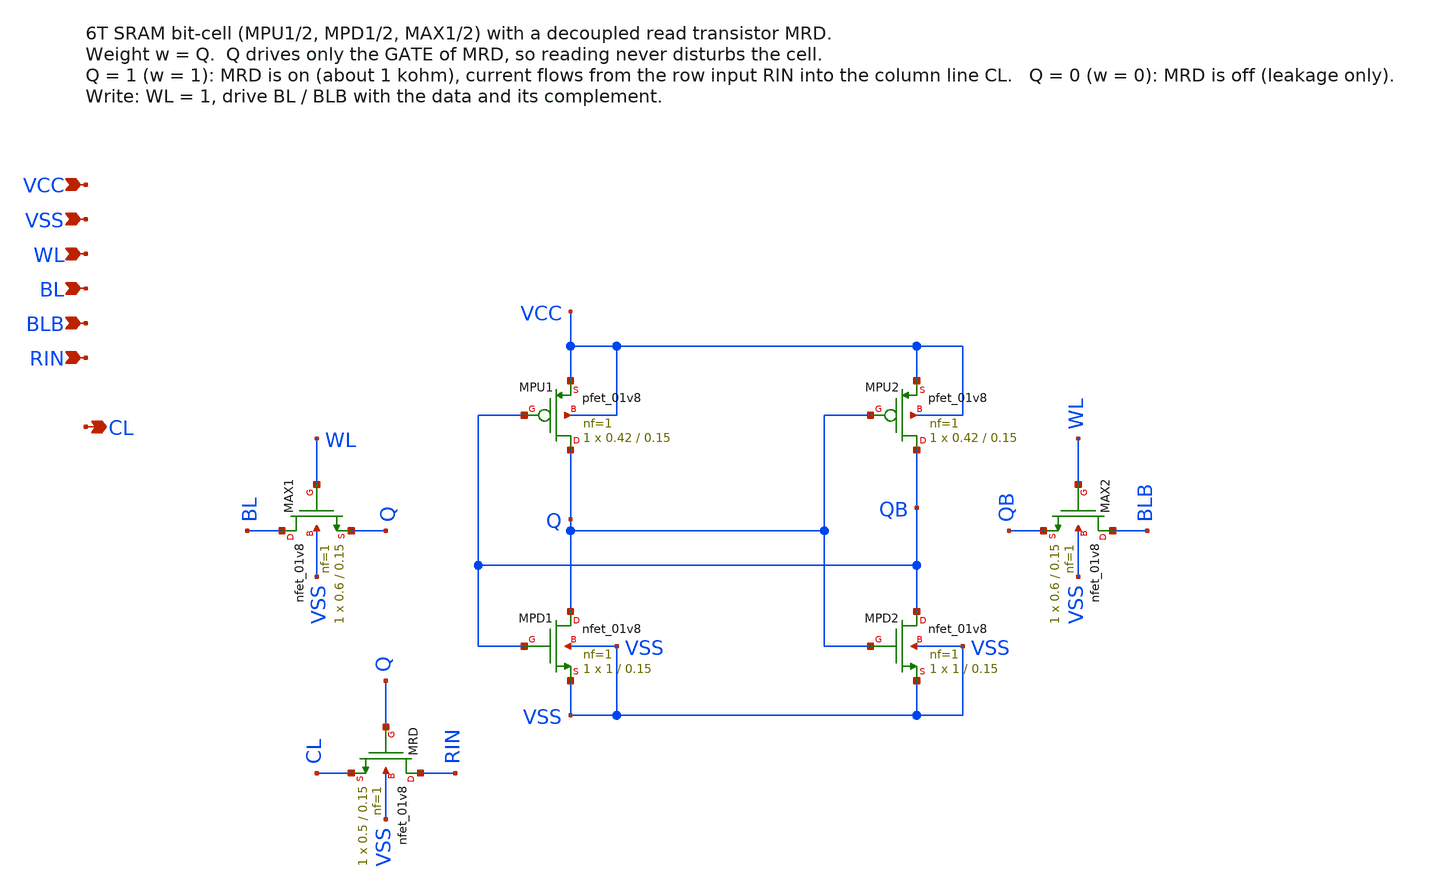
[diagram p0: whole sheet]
** sch_path: CiM components/sram_cell6t.sch
**.subckt sram_cell6t VCC VSS WL BL BLB RIN CL
*.ipin VCC
*.ipin VSS
*.ipin WL
*.ipin BL
*.ipin BLB
*.ipin RIN
*.opin CL
XMPU1 Q QB VCC VCC sky130_fd_pr__pfet_01v8 L=0.15 W=0.42 nf=1 ad='int((nf+1)/2) * W/nf * 0.29' as='int((nf+2)/2) * W/nf * 0.29'
+ pd='2*int((nf+1)/2) * (W/nf + 0.29)' ps='2*int((nf+2)/2) * (W/nf + 0.29)' nrd='0.29 / W' nrs='0.29 / W'
+ sa=0 sb=0 sd=0 mult=1 m=1
XMPU2 QB Q VCC VCC sky130_fd_pr__pfet_01v8 L=0.15 W=0.42 nf=1 ad='int((nf+1)/2) * W/nf * 0.29' as='int((nf+2)/2) * W/nf * 0.29'
+ pd='2*int((nf+1)/2) * (W/nf + 0.29)' ps='2*int((nf+2)/2) * (W/nf + 0.29)' nrd='0.29 / W' nrs='0.29 / W'
+ sa=0 sb=0 sd=0 mult=1 m=1
XMPD1 Q QB VSS VSS sky130_fd_pr__nfet_01v8 L=0.15 W=1 nf=1 ad='int((nf+1)/2) * W/nf * 0.29' as='int((nf+2)/2) * W/nf * 0.29'
+ pd='2*int((nf+1)/2) * (W/nf + 0.29)' ps='2*int((nf+2)/2) * (W/nf + 0.29)' nrd='0.29 / W' nrs='0.29 / W'
+ sa=0 sb=0 sd=0 mult=1 m=1
XMPD2 QB Q VSS VSS sky130_fd_pr__nfet_01v8 L=0.15 W=1 nf=1 ad='int((nf+1)/2) * W/nf * 0.29' as='int((nf+2)/2) * W/nf * 0.29'
+ pd='2*int((nf+1)/2) * (W/nf + 0.29)' ps='2*int((nf+2)/2) * (W/nf + 0.29)' nrd='0.29 / W' nrs='0.29 / W'
+ sa=0 sb=0 sd=0 mult=1 m=1
XMAX1 BL WL Q VSS sky130_fd_pr__nfet_01v8 L=0.15 W=0.6 nf=1 ad='int((nf+1)/2) * W/nf * 0.29' as='int((nf+2)/2) * W/nf * 0.29'
+ pd='2*int((nf+1)/2) * (W/nf + 0.29)' ps='2*int((nf+2)/2) * (W/nf + 0.29)' nrd='0.29 / W' nrs='0.29 / W'
+ sa=0 sb=0 sd=0 mult=1 m=1
XMAX2 BLB WL QB VSS sky130_fd_pr__nfet_01v8 L=0.15 W=0.6 nf=1 ad='int((nf+1)/2) * W/nf * 0.29' as='int((nf+2)/2) * W/nf * 0.29'
+ pd='2*int((nf+1)/2) * (W/nf + 0.29)' ps='2*int((nf+2)/2) * (W/nf + 0.29)' nrd='0.29 / W' nrs='0.29 / W'
+ sa=0 sb=0 sd=0 mult=1 m=1
XMRD RIN Q CL VSS sky130_fd_pr__nfet_01v8 L=0.15 W=0.5 nf=1 ad='int((nf+1)/2) * W/nf * 0.29' as='int((nf+2)/2) * W/nf * 0.29'
+ pd='2*int((nf+1)/2) * (W/nf + 0.29)' ps='2*int((nf+2)/2) * (W/nf + 0.29)' nrd='0.29 / W' nrs='0.29 / W'
+ sa=0 sb=0 sd=0 mult=1 m=1
**.ends
.end
